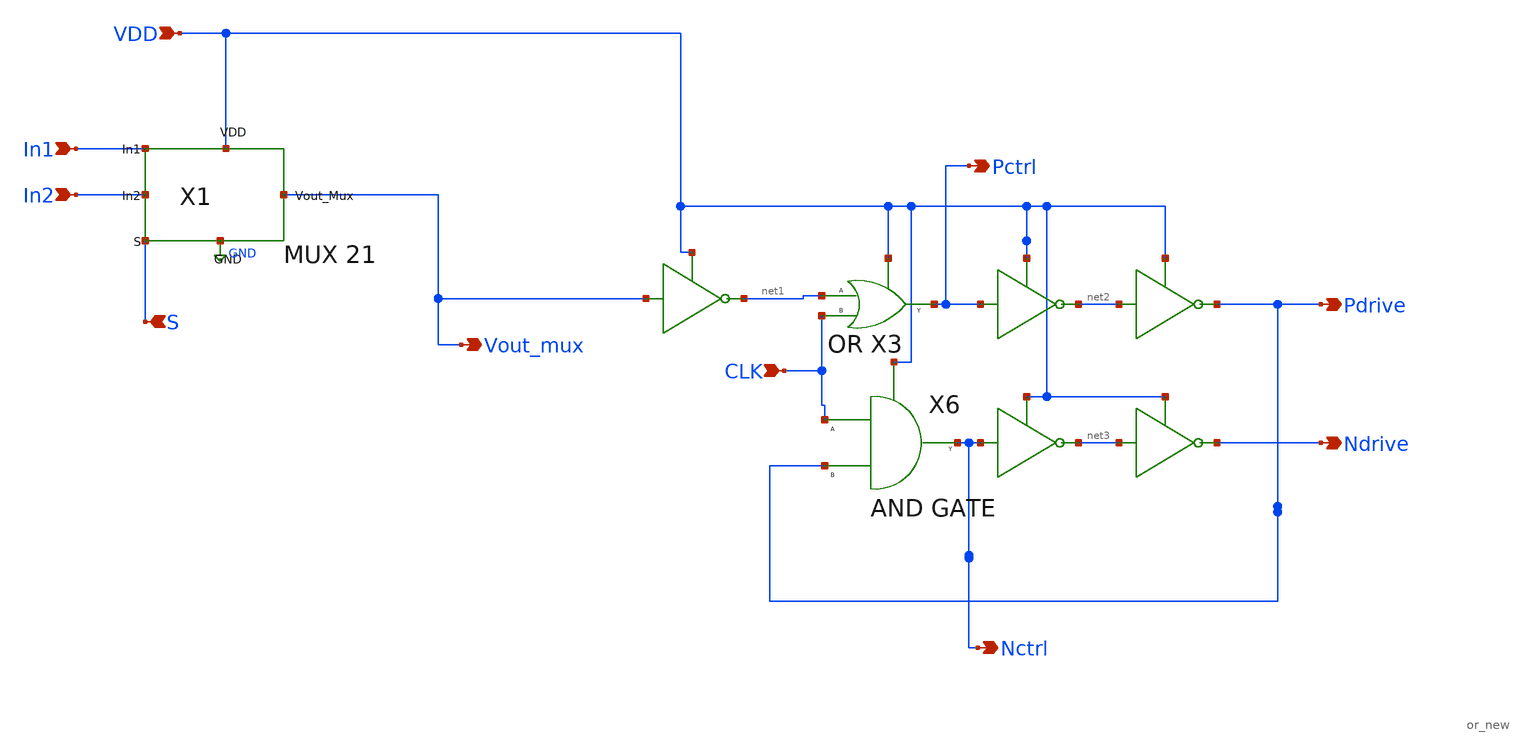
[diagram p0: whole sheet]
** sch_path: Current Sensor/dtc.sch
**.subckt dtc VDD Vout_mux S In1 In2 Pdrive Pctrl Ndrive Nctrl CLK
*.ipin VDD
*.opin Vout_mux
*.ipin S
*.ipin In1
*.ipin In2
*.opin Pdrive
*.opin Pctrl
*.opin Ndrive
*.opin Nctrl
*.ipin CLK
X3 CLK net1 Pctrl VDD or_new
X6 CLK Pdrive Nctrl VDD and
X1 In1 In2 S VDD Vout_mux GND mux21
**.ends
.GLOBAL GND
.end
